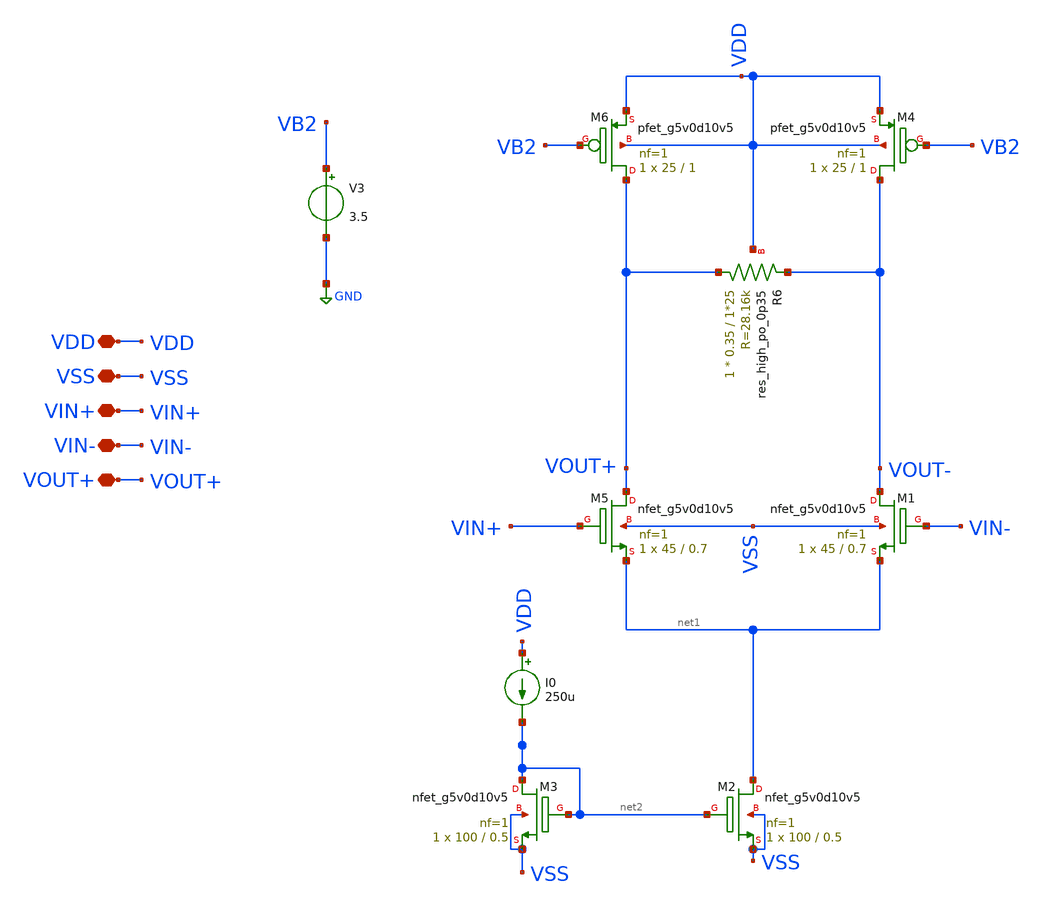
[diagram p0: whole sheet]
** sch_path: amplifiers/differencial_stage_amps/stange stages/current_load/differential_stage.sch
**.subckt differential_stage VDD VSS VIN+ VIN- VOUT+
*.iopin VDD
*.iopin VSS
*.iopin VIN+
*.iopin VIN-
*.iopin VOUT+
XM5 VOUT+ VIN+ net1 VSS sky130_fd_pr__nfet_g5v0d10v5 L=0.7 W=45 nf=1 ad='int((1 + 1)/2) * 45 / 1 * 0.29'
+ as='int((1 + 2)/2) * 45 / 1 * 0.29' pd='2*int((1 + 1)/2) * (45 / 1 + 0.29)' ps='2*int((1 + 2)/2) * (45 / 1 + 0.29)'
+ nrd='0.29 / 45 ' nrs='0.29 / 45 ' sa=0 sb=0 sd=0 mult=1 m=1
XM1 VOUT- VIN- net1 VSS sky130_fd_pr__nfet_g5v0d10v5 L=0.7 W=45 nf=1 ad='int((1 + 1)/2) * 45 / 1 * 0.29'
+ as='int((1 + 2)/2) * 45 / 1 * 0.29' pd='2*int((1 + 1)/2) * (45 / 1 + 0.29)' ps='2*int((1 + 2)/2) * (45 / 1 + 0.29)'
+ nrd='0.29 / 45 ' nrs='0.29 / 45 ' sa=0 sb=0 sd=0 mult=1 m=1
XM2 net1 net2 VSS VSS sky130_fd_pr__nfet_g5v0d10v5 L=0.5 W=100 nf=1 ad='int((1 + 1)/2) * 100 / 1 * 0.29'
+ as='int((1 + 2)/2) * 100 / 1 * 0.29' pd='2*int((1 + 1)/2) * (100 / 1 + 0.29)' ps='2*int((1 + 2)/2) * (100 / 1 + 0.29)'
+ nrd='0.29 / 100 ' nrs='0.29 / 100 ' sa=0 sb=0 sd=0 mult=1 m=1
XM3 net2 net2 VSS VSS sky130_fd_pr__nfet_g5v0d10v5 L=0.5 W=100 nf=1 ad='int((1 + 1)/2) * 100 / 1 * 0.29'
+ as='int((1 + 2)/2) * 100 / 1 * 0.29' pd='2*int((1 + 1)/2) * (100 / 1 + 0.29)' ps='2*int((1 + 2)/2) * (100 / 1 + 0.29)'
+ nrd='0.29 / 100 ' nrs='0.29 / 100 ' sa=0 sb=0 sd=0 mult=1 m=1
I0 VDD net2 250u
XM4 VOUT- VB2 VDD VDD sky130_fd_pr__pfet_g5v0d10v5 L=1 W=25 nf=1 ad='int((1 + 1)/2) * 25 / 1 * 0.29'
+ as='int((1 + 2)/2) * 25 / 1 * 0.29' pd='2*int((1 + 1)/2) * (25 / 1 + 0.29)' ps='2*int((1 + 2)/2) * (25 / 1 + 0.29)'
+ nrd='0.29 / 25 ' nrs='0.29 / 25 ' sa=0 sb=0 sd=0 mult=1 m=1
XR6 VOUT+ VOUT- VDD sky130_fd_pr__res_high_po_0p35 L=1*25 mult=1 m=1
XM6 VOUT+ VB2 VDD VDD sky130_fd_pr__pfet_g5v0d10v5 L=1 W=25 nf=1 ad='int((1 + 1)/2) * 25 / 1 * 0.29'
+ as='int((1 + 2)/2) * 25 / 1 * 0.29' pd='2*int((1 + 1)/2) * (25 / 1 + 0.29)' ps='2*int((1 + 2)/2) * (25 / 1 + 0.29)'
+ nrd='0.29 / 25 ' nrs='0.29 / 25 ' sa=0 sb=0 sd=0 mult=1 m=1
V3 VB2 GND 3.5
**.ends
.GLOBAL GND
.end
